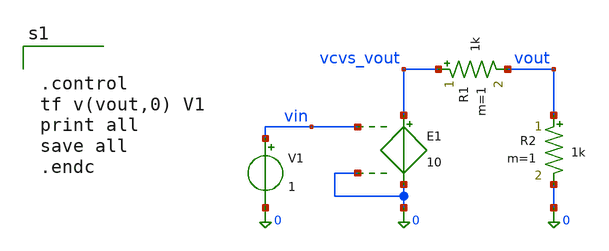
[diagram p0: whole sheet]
** sch_path: mag/layout/vcvs_example.sch
**.subckt vcvs_example
E1 vcvs_vout 0 vin 0 10
V1 vin 0 1
R1 vcvs_vout vout 1k m=1
R2 vout 0 1k m=1
**** begin user architecture code


.control
tf v(vout,0) V1
print all
save all
.endc

**** end user architecture code
**.ends
.end
